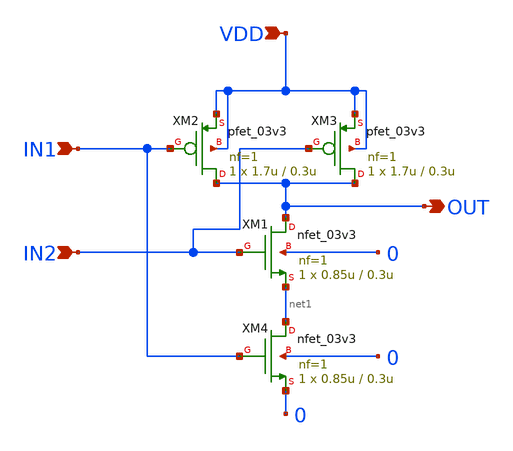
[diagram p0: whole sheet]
** sch_path: initial_notebooks_2023/Current-Steering DAC/DAC/NAND2_1.sch
**.subckt NAND2_1 OUT IN1 IN2 VDD
*.opin OUT
*.ipin IN1
*.ipin IN2
*.ipin VDD
XM1 OUT IN2 net1 0 nfet_03v3 L=0.3u W=0.85u nf=1 ad='int((nf+1)/2) * W/nf * 0.18u' as='int((nf+2)/2) * W/nf * 0.18u'
+ pd='2*int((nf+1)/2) * (W/nf + 0.18u)' ps='2*int((nf+2)/2) * (W/nf + 0.18u)' nrd='0.18u / W' nrs='0.18u / W'
+ sa=0 sb=0 sd=0 m=1
XM2 OUT IN1 VDD VDD pfet_03v3 L=0.3u W=1.7u nf=1 ad='int((nf+1)/2) * W/nf * 0.18u' as='int((nf+2)/2) * W/nf * 0.18u'
+ pd='2*int((nf+1)/2) * (W/nf + 0.18u)' ps='2*int((nf+2)/2) * (W/nf + 0.18u)' nrd='0.18u / W' nrs='0.18u / W'
+ sa=0 sb=0 sd=0 m=1
XM3 OUT IN2 VDD VDD pfet_03v3 L=0.3u W=1.7u nf=1 ad='int((nf+1)/2) * W/nf * 0.18u' as='int((nf+2)/2) * W/nf * 0.18u'
+ pd='2*int((nf+1)/2) * (W/nf + 0.18u)' ps='2*int((nf+2)/2) * (W/nf + 0.18u)' nrd='0.18u / W' nrs='0.18u / W'
+ sa=0 sb=0 sd=0 m=1
XM4 net1 IN1 0 0 nfet_03v3 L=0.3u W=0.85u nf=1 ad='int((nf+1)/2) * W/nf * 0.18u' as='int((nf+2)/2) * W/nf * 0.18u'
+ pd='2*int((nf+1)/2) * (W/nf + 0.18u)' ps='2*int((nf+2)/2) * (W/nf + 0.18u)' nrd='0.18u / W' nrs='0.18u / W'
+ sa=0 sb=0 sd=0 m=1
**.ends
.end
